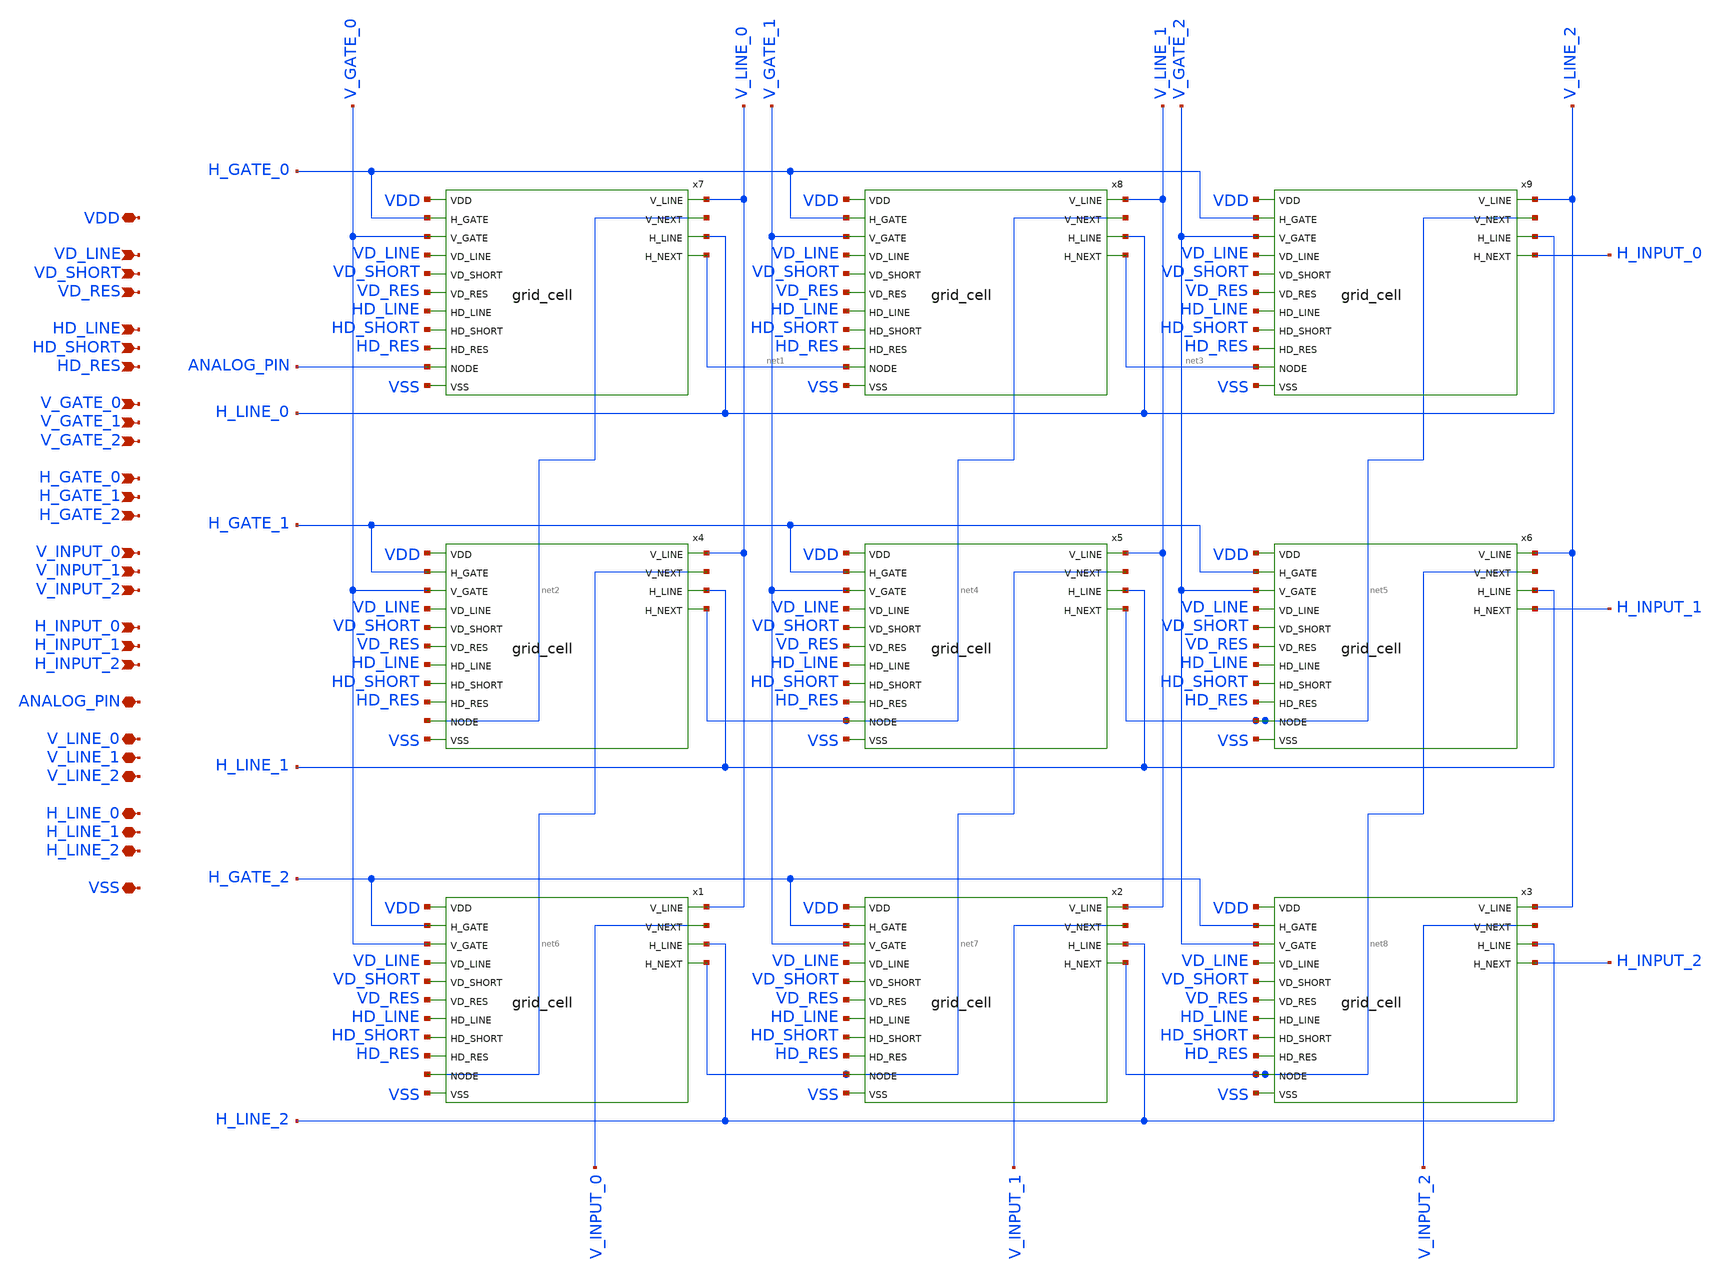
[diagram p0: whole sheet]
** sch_path: xschem/mini_grid.sch
**.subckt mini_grid V_INPUT_0 V_INPUT_1 V_INPUT_2 H_INPUT_0 H_INPUT_1 H_INPUT_2 V_GATE_0 V_GATE_1
*+ V_GATE_2 H_GATE_0 H_GATE_1 H_GATE_2 ANALOG_PIN VSS VDD VD_LINE VD_SHORT VD_RES HD_LINE HD_SHORT HD_RES
*+ V_LINE_0 V_LINE_1 V_LINE_2 H_LINE_0 H_LINE_1 H_LINE_2
*.ipin V_INPUT_0
*.ipin V_INPUT_1
*.ipin V_INPUT_2
*.ipin H_INPUT_0
*.ipin H_INPUT_1
*.ipin H_INPUT_2
*.ipin V_GATE_0
*.ipin V_GATE_1
*.ipin V_GATE_2
*.ipin H_GATE_0
*.ipin H_GATE_1
*.ipin H_GATE_2
*.iopin ANALOG_PIN
*.iopin VSS
*.iopin VDD
*.ipin VD_LINE
*.ipin VD_SHORT
*.ipin VD_RES
*.ipin HD_LINE
*.ipin HD_SHORT
*.ipin HD_RES
*.iopin V_LINE_0
*.iopin V_LINE_1
*.iopin V_LINE_2
*.iopin H_LINE_0
*.iopin H_LINE_1
*.iopin H_LINE_2
x1 VDD H_GATE_2 V_GATE_0 V_LINE_0 VD_LINE V_INPUT_0 VD_SHORT VD_RES H_LINE_2 HD_LINE net7 HD_SHORT
+ HD_RES net6 VSS grid_cell
x2 VDD H_GATE_2 V_GATE_1 V_LINE_1 VD_LINE V_INPUT_1 VD_SHORT VD_RES H_LINE_2 HD_LINE net8 HD_SHORT
+ HD_RES net7 VSS grid_cell
x3 VDD H_GATE_2 V_GATE_2 V_LINE_2 VD_LINE V_INPUT_2 VD_SHORT VD_RES H_LINE_2 HD_LINE H_INPUT_2
+ HD_SHORT HD_RES net8 VSS grid_cell
x4 VDD H_GATE_1 V_GATE_0 V_LINE_0 VD_LINE net6 VD_SHORT VD_RES H_LINE_1 HD_LINE net4 HD_SHORT HD_RES
+ net2 VSS grid_cell
x5 VDD H_GATE_1 V_GATE_1 V_LINE_1 VD_LINE net7 VD_SHORT VD_RES H_LINE_1 HD_LINE net5 HD_SHORT HD_RES
+ net4 VSS grid_cell
x6 VDD H_GATE_1 V_GATE_2 V_LINE_2 VD_LINE net8 VD_SHORT VD_RES H_LINE_1 HD_LINE H_INPUT_1 HD_SHORT
+ HD_RES net5 VSS grid_cell
x7 VDD H_GATE_0 V_GATE_0 V_LINE_0 VD_LINE net2 VD_SHORT VD_RES H_LINE_0 HD_LINE net1 HD_SHORT HD_RES
+ ANALOG_PIN VSS grid_cell
x8 VDD H_GATE_0 V_GATE_1 V_LINE_1 VD_LINE net4 VD_SHORT VD_RES H_LINE_0 HD_LINE net3 HD_SHORT HD_RES
+ net1 VSS grid_cell
x9 VDD H_GATE_0 V_GATE_2 V_LINE_2 VD_LINE net5 VD_SHORT VD_RES H_LINE_0 HD_LINE H_INPUT_0 HD_SHORT
+ HD_RES net3 VSS grid_cell
**.ends
.end
